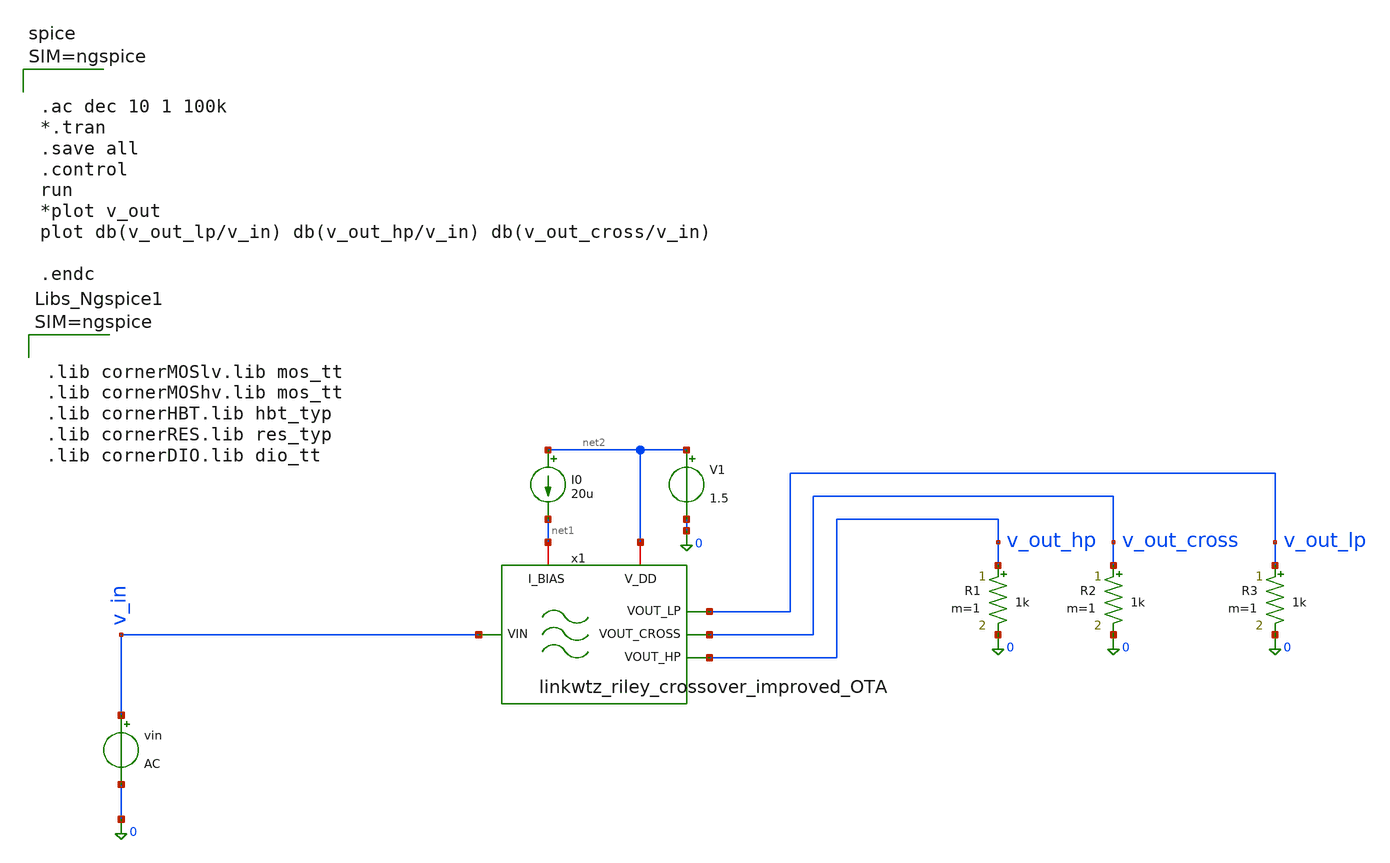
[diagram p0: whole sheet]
** sch_path: 004_Real_Circuits/linkwitz_riley_real_circ_top_tb.sch
**.subckt linkwitz_riley_real_circ_top_tb
vin v_in 0 AC
R2 v_out_cross 0 1k m=1
R3 v_out_lp 0 1k m=1
x1 net2 net1 v_out_lp v_in v_out_cross v_out_hp linkwtz_riley_crossover_improved_OTA
I0 net2 net1 20u
V1 net2 0 1.5
R1 v_out_hp 0 1k m=1
**** begin user architecture code



.lib cornerMOSlv.lib mos_tt
.lib cornerMOShv.lib mos_tt
.lib cornerHBT.lib hbt_typ
.lib cornerRES.lib res_typ
.lib cornerDIO.lib dio_tt






.ac dec 10 1 100k
*.tran
.save all
.control
run
*plot v_out
plot db(v_out_lp/v_in) db(v_out_hp/v_in) db(v_out_cross/v_in)

.endc



**** end user architecture code
**.ends

* expanding   symbol:  /foss/designs/Repo/004_Real_Circuits/linkwtz_riley_crossover_improved_OTA.sym
*+ # of pins=6
** sym_path: 004_Real_Circuits/linkwtz_riley_crossover_improved_OTA.sym
** sch_path: 004_Real_Circuits/linkwtz_riley_crossover_improved_OTA.sch
.subckt linkwtz_riley_crossover_improved_OTA V_DD I_BIAS VOUT_LP VIN VOUT_CROSS VOUT_HP
*.opin VOUT_LP
*.opin VOUT_HP
*.ipin VIN
*.iopin I_BIAS
*.iopin V_DD
*.opin VOUT_CROSS
x1 V_DD VOUT_LP I_BIAS net2 VOUT_LP 0 5T-OTA
x2 V_DD VOUT_HP I_BIAS net4 VOUT_HP 0 5T-OTA
R1 net1 VIN R_LP m=1
.param C_LP=1.06e-6
.param R_LP=1000
.param C_HP=1e-9
.param R_HP=1.06e6
.param R_IN=1k
R2 net2 net1 R_LP m=1
C1 net2 0 C_LP m=1
C2 net1 VOUT_LP C_LP m=1
C3 VIN net3 C_HP m=1
C4 net3 net4 C_HP m=1
R3 net3 VOUT_HP R_HP m=1
R4 net4 0 R_HP m=1
R10 net5 net6 R_IN m=1
R11 VOUT_HP net5 R_IN m=1
R12 net7 VOUT_CROSS R_IN m=1
R13 net6 net7 R_IN m=1
R14 VOUT_LP net7 R_IN m=1
E1 net6 0 0 net5 1e6
E4 VOUT_CROSS 0 0 net7 1e6
.ends


* expanding   symbol:  /foss/designs/Repo/004_Real_Circuits/5T-OTA.sym # of pins=6
** sym_path: 004_Real_Circuits/5T-OTA.sym
** sch_path: 004_Real_Circuits/5T-OTA.sch
.subckt 5T-OTA vdd vout ibias vinp vinn vss
*.ipin vinp
*.iopin vdd
*.iopin vss
*.opin vout
*.ipin vinn
*.iopin ibias
XM1 vb vinp vt vt sg13_lv_nmos w=M12_W l=5u ng=1 m=1 mm_ok=1
XM5 vt ibias vss vss sg13_lv_nmos w=M5_W l=5u ng=1 m=1 mm_ok=1
XM2 vout vinn vt vt sg13_lv_nmos w=M12_W l=5u ng=1 m=1 mm_ok=1
XM6 ibias ibias vss vss sg13_lv_nmos w=M6_W l=5u ng=1 m=1 mm_ok=1
XM3 vb vb vdd vdd sg13_lv_pmos w=M34_W l=5u ng=1 m=1 mm_ok=1
XM4 vout vb vdd vdd sg13_lv_pmos w=M34_W l=5u ng=1 m=1 mm_ok=1
.param M34_W=3.5u
.param M12_W=2u
.param M5_W=1.5u
.param M6_W=7.5u
.ends

.end
